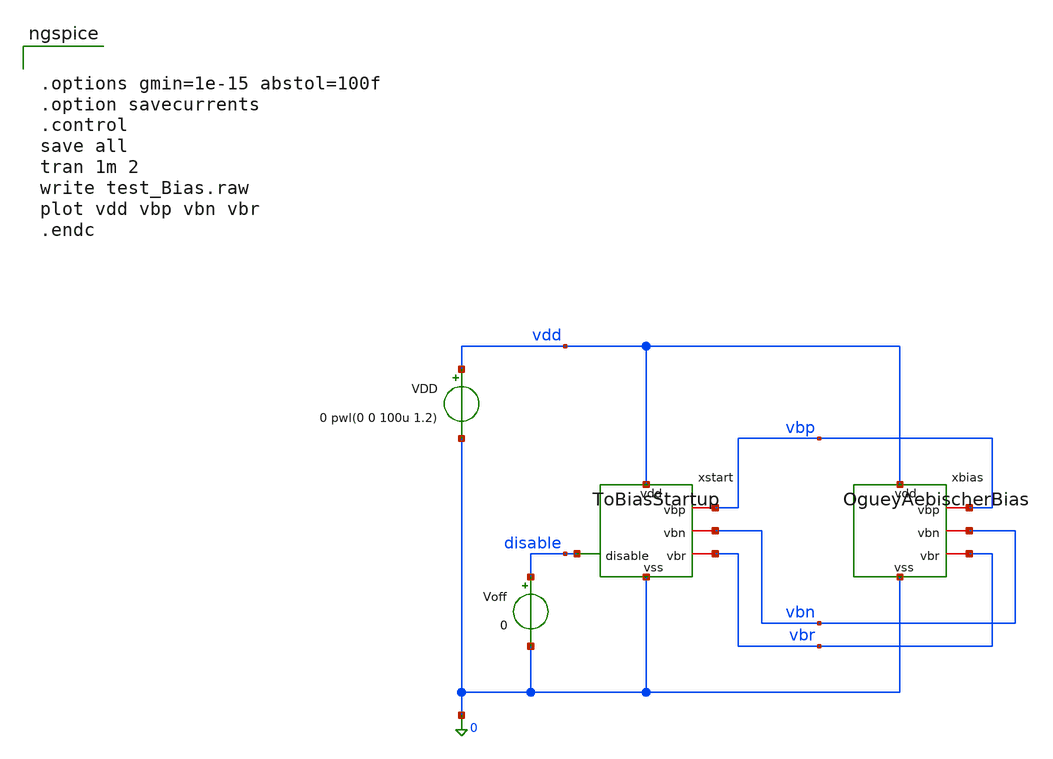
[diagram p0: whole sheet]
** sch_path: playground/test_Bias.sch
**.subckt test_Bias
xbias vdd vbp vbn vbr 0 OgueyAebischerBias
xstart vdd vbp vbn disable vbr 0 ToBiasStartup
VDD vdd 0 0 pwl(0 0 100u 1.2)
Voff disable 0 0
**** begin user architecture code


.options gmin=1e-15 abstol=100f
.option savecurrents
.control
save all
tran 1m 2
write test_Bias.raw
plot vdd vbp vbn vbr
.endc


 .lib $::SKYWATER_MODELS/models/sky130.lib.spice tt

.param mc_mm_switch=0
.param mc_pr_switch=1


**** end user architecture code
**.ends

* expanding   symbol:  OgueyAebischerBias.sym # of pins=5
** sym_path: OgueyAebischerBias.sym
** sch_path: OgueyAebischerBias.sch
.subckt OgueyAebischerBias vdd vbp vbn vbr vss
*.iopin vss
*.iopin vdd
*.iopin vbp
*.iopin vbn
*.iopin vbr
XM10 vbp vbn net1 vss sky130_fd_pr__nfet_01v8 L=20 W=1 nf=1 ad='int((1 + 1)/2) * 1 / 1 * 0.29' as='int((1 + 2)/2) * 1 / 1 * 0.29'
+ pd='2*int((1 + 1)/2) * (1 / 1 + 0.29)' ps='2*int((1 + 2)/2) * (1 / 1 + 0.29)' nrd='0.29 / 1 ' nrs='0.29 / 1 '
+ sa=0 sb=0 sd=0 mult=1 m=1
XM12 vbp vbp vdd vdd sky130_fd_pr__pfet_01v8 L=20 W=1 nf=1 ad='int((nf+1)/2) * W/nf * 0.29' as='int((nf+2)/2) * W/nf * 0.29'
+ pd='2*int((nf+1)/2) * (W/nf + 0.29)' ps='2*int((nf+2)/2) * (W/nf + 0.29)' nrd='0.29 / W' nrs='0.29 / W'
+ sa=0 sb=0 sd=0 mult=1 m=1
XM11 vbn vbn vss vss sky130_fd_pr__nfet_01v8 L=20 W=1 nf=1 ad='int((1 + 1)/2) * 1 / 1 * 0.29' as='int((1 + 2)/2) * 1 / 1 * 0.29'
+ pd='2*int((1 + 1)/2) * (1 / 1 + 0.29)' ps='2*int((1 + 2)/2) * (1 / 1 + 0.29)' nrd='0.29 / 1 ' nrs='0.29 / 1 '
+ sa=0 sb=0 sd=0 mult=4 m=4
XM13 vbn vbp vdd vdd sky130_fd_pr__pfet_01v8 L=20 W=1 nf=1 ad='int((nf+1)/2) * W/nf * 0.29' as='int((nf+2)/2) * W/nf * 0.29'
+ pd='2*int((nf+1)/2) * (W/nf + 0.29)' ps='2*int((nf+2)/2) * (W/nf + 0.29)' nrd='0.29 / W' nrs='0.29 / W'
+ sa=0 sb=0 sd=0 mult=4 m=4
XM14 vbr vbp vdd vdd sky130_fd_pr__pfet_01v8 L=20 W=1 nf=1 ad='int((nf+1)/2) * W/nf * 0.29' as='int((nf+2)/2) * W/nf * 0.29'
+ pd='2*int((nf+1)/2) * (W/nf + 0.29)' ps='2*int((nf+2)/2) * (W/nf + 0.29)' nrd='0.29 / W' nrs='0.29 / W'
+ sa=0 sb=0 sd=0 mult=1 m=1
XM16 net1 vbr vss vss sky130_fd_pr__nfet_01v8 L=100 W=1 nf=1 ad='int((1 + 1)/2) * 1 / 1 * 0.29' as='int((1 + 2)/2) * 1 / 1 * 0.29'
+ pd='2*int((1 + 1)/2) * (1 / 1 + 0.29)' ps='2*int((1 + 2)/2) * (1 / 1 + 0.29)' nrd='0.29 / 1 ' nrs='0.29 / 1 '
+ sa=0 sb=0 sd=0 mult=1 m=1
XM15 vbr vbr vss vss sky130_fd_pr__nfet_01v8 L=100 W=1 nf=1 ad='int((1 + 1)/2) * 1 / 1 * 0.29' as='int((1 + 2)/2) * 1 / 1 * 0.29'
+ pd='2*int((1 + 1)/2) * (1 / 1 + 0.29)' ps='2*int((1 + 2)/2) * (1 / 1 + 0.29)' nrd='0.29 / 1 ' nrs='0.29 / 1 '
+ sa=0 sb=0 sd=0 mult=1 m=1
.ends


* expanding   symbol:  ToBiasStartup.sym # of pins=6
** sym_path: ToBiasStartup.sym
** sch_path: ToBiasStartup.sch
.subckt ToBiasStartup vdd vbp vbn disable vbr vss
*.iopin vss
*.iopin vdd
*.iopin vbp
*.iopin vbn
*.iopin vbr
*.ipin disable
XM24 vbr disable vss vss sky130_fd_pr__nfet_01v8 L=0.3 W=1 nf=1 ad='int((1 + 1)/2) * 1 / 1 * 0.29' as='int((1 + 2)/2) * 1 / 1 * 0.29'
+ pd='2*int((1 + 1)/2) * (1 / 1 + 0.29)' ps='2*int((1 + 2)/2) * (1 / 1 + 0.29)' nrd='0.29 / 1 ' nrs='0.29 / 1 '
+ sa=0 sb=0 sd=0 mult=1 m=1
XM22 vbr vkick vdd vdd sky130_fd_pr__pfet_01v8 L=0.3 W=1 nf=1 ad='int((nf+1)/2) * W/nf * 0.29' as='int((nf+2)/2) * W/nf * 0.29'
+ pd='2*int((nf+1)/2) * (W/nf + 0.29)' ps='2*int((nf+2)/2) * (W/nf + 0.29)' nrd='0.29 / W' nrs='0.29 / W'
+ sa=0 sb=0 sd=0 mult=1 m=1
XM25 vkick vbp vdd vdd sky130_fd_pr__pfet_01v8 L=0.3 W=1 nf=1 ad='int((nf+1)/2) * W/nf * 0.29' as='int((nf+2)/2) * W/nf * 0.29'
+ pd='2*int((nf+1)/2) * (W/nf + 0.29)' ps='2*int((nf+2)/2) * (W/nf + 0.29)' nrd='0.29 / W' nrs='0.29 / W'
+ sa=0 sb=0 sd=0 mult=1 m=1
XM23 vbn disable vss vss sky130_fd_pr__nfet_01v8 L=0.3 W=1 nf=1 ad='int((1 + 1)/2) * 1 / 1 * 0.29' as='int((1 + 2)/2) * 1 / 1 * 0.29'
+ pd='2*int((1 + 1)/2) * (1 / 1 + 0.29)' ps='2*int((1 + 2)/2) * (1 / 1 + 0.29)' nrd='0.29 / 1 ' nrs='0.29 / 1 '
+ sa=0 sb=0 sd=0 mult=1 m=1
XM21 vbn vkick vdd vdd sky130_fd_pr__pfet_01v8 L=0.3 W=1 nf=1 ad='int((nf+1)/2) * W/nf * 0.29' as='int((nf+2)/2) * W/nf * 0.29'
+ pd='2*int((nf+1)/2) * (W/nf + 0.29)' ps='2*int((nf+2)/2) * (W/nf + 0.29)' nrd='0.29 / W' nrs='0.29 / W'
+ sa=0 sb=0 sd=0 mult=1 m=1
XM20 disable vkick disable vss sky130_fd_pr__nfet_01v8 L=40 W=40 nf=1 ad='int((1 + 1)/2) * 40 / 1 * 0.29'
+ as='int((1 + 2)/2) * 40 / 1 * 0.29' pd='2*int((1 + 1)/2) * (40 / 1 + 0.29)' ps='2*int((1 + 2)/2) * (40 / 1 + 0.29)'
+ nrd='0.29 / 40 ' nrs='0.29 / 40 ' sa=0 sb=0 sd=0 mult=1 m=1
XM26 vdd vbp vdd vss sky130_fd_pr__nfet_01v8 L=40 W=40 nf=1 ad='int((1 + 1)/2) * 40 / 1 * 0.29' as='int((1 + 2)/2) * 40 / 1 * 0.29'
+ pd='2*int((1 + 1)/2) * (40 / 1 + 0.29)' ps='2*int((1 + 2)/2) * (40 / 1 + 0.29)' nrd='0.29 / 40 ' nrs='0.29 / 40 '
+ sa=0 sb=0 sd=0 mult=1 m=1
.ends

.end
